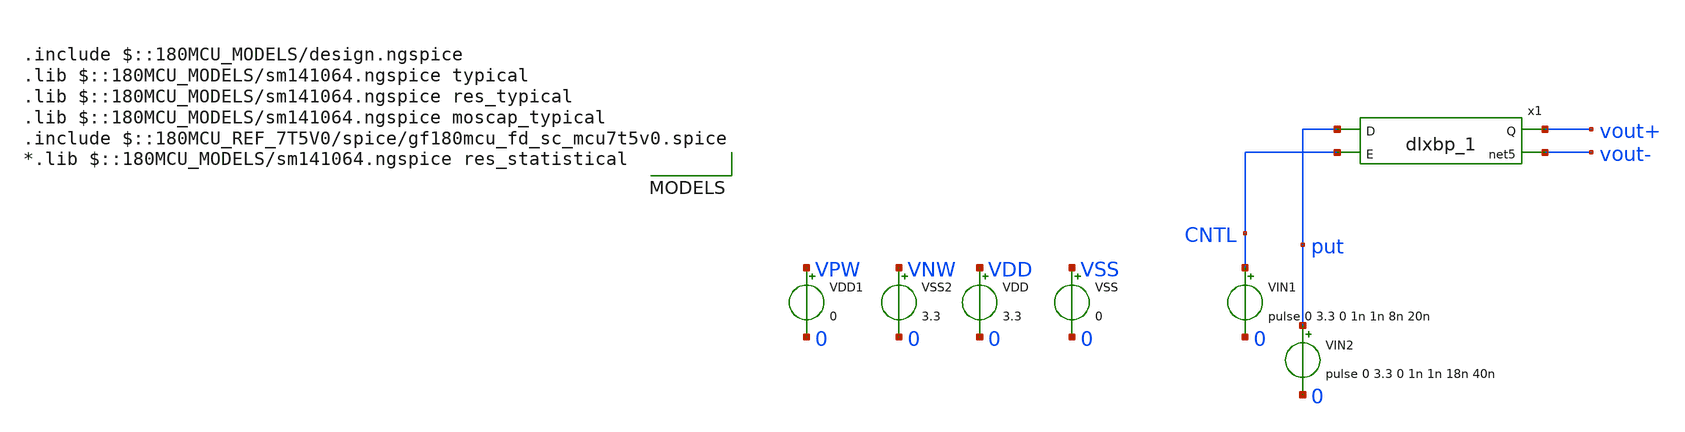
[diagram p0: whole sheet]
** sch_path: DAC/xschem/std_cell/Test_dffqnq.sch
**.subckt Test_dffqnq
VIN1 CNTL 0 pulse 0 3.3 0 1n 1n 8n 20n
VIN2 put 0 pulse 0 3.3 0 1n 1n 18n 40n
VDD VDD 0 3.3
VSS VSS 0 0
VDD1 VPW 0 0
VSS2 VNW 0 3.3
x1 put CNTL vout+ vout- VDD VNW VPW VSS gf180mcu_fd_sc_mcu7t5v0__latqnq_1
**** begin user architecture code

.include $::180MCU_MODELS/design.ngspice
.lib $::180MCU_MODELS/sm141064.ngspice typical
.lib $::180MCU_MODELS/sm141064.ngspice res_typical
.lib $::180MCU_MODELS/sm141064.ngspice moscap_typical
.include $::180MCU_REF_7T5V0/spice/gf180mcu_fd_sc_mcu7t5v0.spice
*.lib $::180MCU_MODELS/sm141064.ngspice res_statistical





.control
	*tran interval duration
	tran 1n 100n

	*dc vin1 0 3.3 0.1
	plot v(CNTL) V(put) v(vout+) v(vout-)
	plot v(vout+) v(vout-)
	write test_and.raw

.endc
.save all




**** end user architecture code
**.ends
.end
